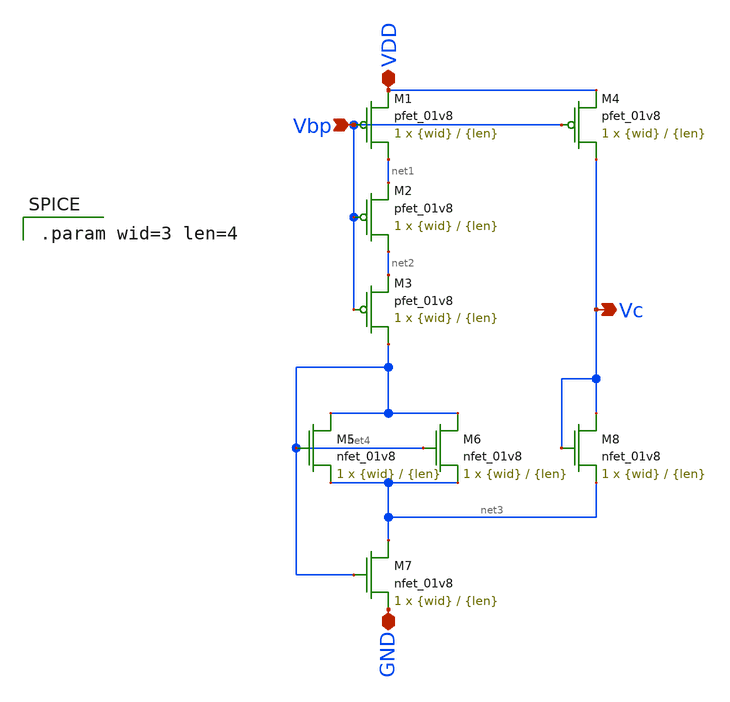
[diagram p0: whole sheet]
** sch_path: mp3/cascode_bias.sch
**.subckt cascode_bias Vbp VDD GND Vc
*.ipin Vbp
*.iopin VDD
*.iopin GND
*.opin Vc
XM1 net1 Vbp VDD VDD sky130_fd_pr__pfet_01v8 L={len} W={wid} nf=1 ad='int((nf+1)/2) * W/nf * 0.29' as='int((nf+2)/2) * W/nf * 0.29'
+ pd='2*int((nf+1)/2) * (W/nf + 0.29)' ps='2*int((nf+2)/2) * (W/nf + 0.29)' nrd='0.29 / W' nrs='0.29 / W'
+ sa=0 sb=0 sd=0 mult=1 m=1
XM2 net2 Vbp net1 VDD sky130_fd_pr__pfet_01v8 L={len} W={wid} nf=1 ad='int((nf+1)/2) * W/nf * 0.29' as='int((nf+2)/2) * W/nf * 0.29'
+ pd='2*int((nf+1)/2) * (W/nf + 0.29)' ps='2*int((nf+2)/2) * (W/nf + 0.29)' nrd='0.29 / W' nrs='0.29 / W'
+ sa=0 sb=0 sd=0 mult=1 m=1
XM3 net4 Vbp net2 VDD sky130_fd_pr__pfet_01v8 L={len} W={wid} nf=1 ad='int((nf+1)/2) * W/nf * 0.29' as='int((nf+2)/2) * W/nf * 0.29'
+ pd='2*int((nf+1)/2) * (W/nf + 0.29)' ps='2*int((nf+2)/2) * (W/nf + 0.29)' nrd='0.29 / W' nrs='0.29 / W'
+ sa=0 sb=0 sd=0 mult=1 m=1
XM4 Vc Vbp VDD VDD sky130_fd_pr__pfet_01v8 L={len} W={wid} nf=1 ad='int((nf+1)/2) * W/nf * 0.29' as='int((nf+2)/2) * W/nf * 0.29'
+ pd='2*int((nf+1)/2) * (W/nf + 0.29)' ps='2*int((nf+2)/2) * (W/nf + 0.29)' nrd='0.29 / W' nrs='0.29 / W'
+ sa=0 sb=0 sd=0 mult=1 m=1
XM5 net4 net4 net3 GND sky130_fd_pr__nfet_01v8 L={len} W={wid} nf=1 ad='int((nf+1)/2) * W/nf * 0.29'
+ as='int((nf+2)/2) * W/nf * 0.29' pd='2*int((nf+1)/2) * (W/nf + 0.29)' ps='2*int((nf+2)/2) * (W/nf + 0.29)'
+ nrd='0.29 / W' nrs='0.29 / W' sa=0 sb=0 sd=0 mult=1 m=1
XM6 net4 net4 net3 GND sky130_fd_pr__nfet_01v8 L={len} W={wid} nf=1 ad='int((nf+1)/2) * W/nf * 0.29'
+ as='int((nf+2)/2) * W/nf * 0.29' pd='2*int((nf+1)/2) * (W/nf + 0.29)' ps='2*int((nf+2)/2) * (W/nf + 0.29)'
+ nrd='0.29 / W' nrs='0.29 / W' sa=0 sb=0 sd=0 mult=1 m=1
XM7 net3 net4 GND GND sky130_fd_pr__nfet_01v8 L={len} W={wid} nf=1 ad='int((nf+1)/2) * W/nf * 0.29' as='int((nf+2)/2) * W/nf * 0.29'
+ pd='2*int((nf+1)/2) * (W/nf + 0.29)' ps='2*int((nf+2)/2) * (W/nf + 0.29)' nrd='0.29 / W' nrs='0.29 / W'
+ sa=0 sb=0 sd=0 mult=1 m=1
XM8 Vc Vc net3 GND sky130_fd_pr__nfet_01v8 L={len} W={wid} nf=1 ad='int((nf+1)/2) * W/nf * 0.29' as='int((nf+2)/2) * W/nf * 0.29'
+ pd='2*int((nf+1)/2) * (W/nf + 0.29)' ps='2*int((nf+2)/2) * (W/nf + 0.29)' nrd='0.29 / W' nrs='0.29 / W'
+ sa=0 sb=0 sd=0 mult=1 m=1
**** begin user architecture code

.param wid=3 len=4

**** end user architecture code
**.ends
.end
